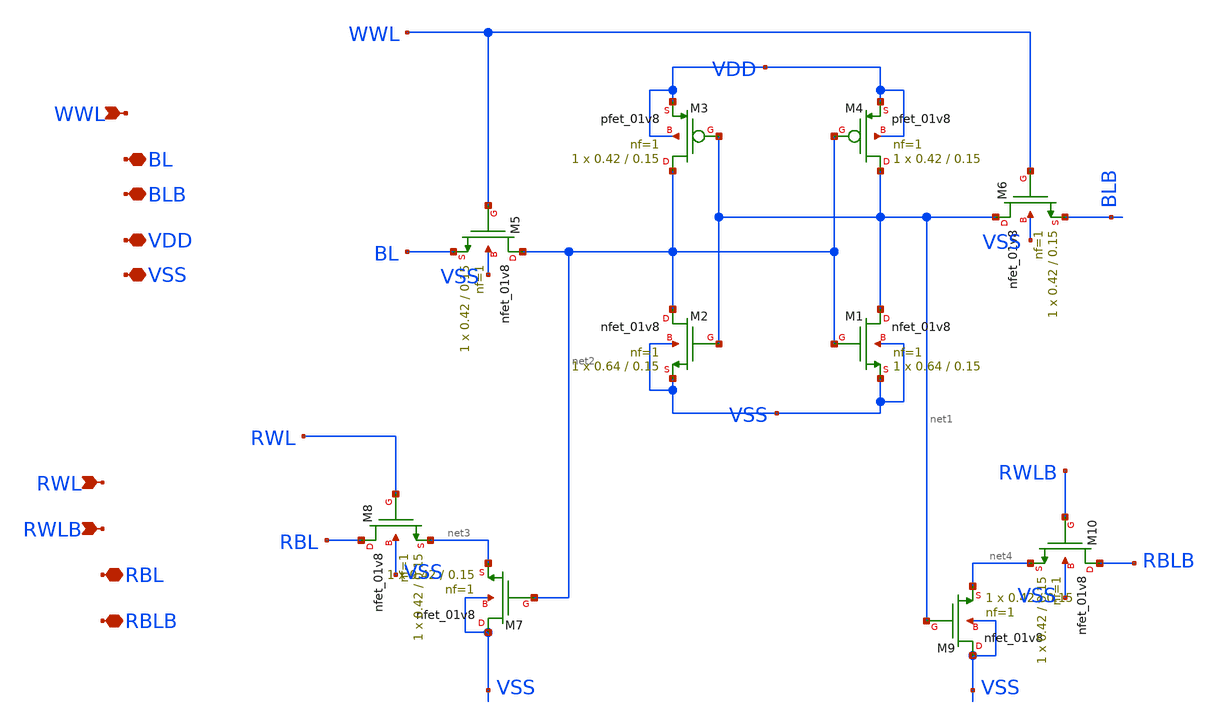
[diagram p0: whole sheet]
** sch_path: xschem/Integrated_bitcell/10T_SRAM_bitcell.sch
**.subckt 10T_SRAM_bitcell BL BLB VDD VSS RBL RBLB WWL RWL RWLB
*.iopin BL
*.iopin BLB
*.iopin VDD
*.iopin VSS
*.iopin RBL
*.iopin RBLB
*.ipin WWL
*.ipin RWL
*.ipin RWLB
XM1 net1 net2 VSS VSS sky130_fd_pr__nfet_01v8 L=0.15 W=0.64 nf=1 ad='int((nf+1)/2) * W/nf * 0.29' as='int((nf+2)/2) * W/nf * 0.29'
+ pd='2*int((nf+1)/2) * (W/nf + 0.29)' ps='2*int((nf+2)/2) * (W/nf + 0.29)' nrd='0.29 / W' nrs='0.29 / W'
+ sa=0 sb=0 sd=0 mult=1 m=1
XM2 net2 net1 VSS VSS sky130_fd_pr__nfet_01v8 L=0.15 W=0.64 nf=1 ad='int((nf+1)/2) * W/nf * 0.29' as='int((nf+2)/2) * W/nf * 0.29'
+ pd='2*int((nf+1)/2) * (W/nf + 0.29)' ps='2*int((nf+2)/2) * (W/nf + 0.29)' nrd='0.29 / W' nrs='0.29 / W'
+ sa=0 sb=0 sd=0 mult=1 m=1
XM3 net2 net1 VDD VDD sky130_fd_pr__pfet_01v8 L=0.15 W=0.42 nf=1 ad='int((nf+1)/2) * W/nf * 0.29' as='int((nf+2)/2) * W/nf * 0.29'
+ pd='2*int((nf+1)/2) * (W/nf + 0.29)' ps='2*int((nf+2)/2) * (W/nf + 0.29)' nrd='0.29 / W' nrs='0.29 / W'
+ sa=0 sb=0 sd=0 mult=1 m=1
XM4 net1 net2 VDD VDD sky130_fd_pr__pfet_01v8 L=0.15 W=0.42 nf=1 ad='int((nf+1)/2) * W/nf * 0.29' as='int((nf+2)/2) * W/nf * 0.29'
+ pd='2*int((nf+1)/2) * (W/nf + 0.29)' ps='2*int((nf+2)/2) * (W/nf + 0.29)' nrd='0.29 / W' nrs='0.29 / W'
+ sa=0 sb=0 sd=0 mult=1 m=1
XM6 net1 WWL BLB VSS sky130_fd_pr__nfet_01v8 L=0.15 W=0.42 nf=1 ad='int((nf+1)/2) * W/nf * 0.29' as='int((nf+2)/2) * W/nf * 0.29'
+ pd='2*int((nf+1)/2) * (W/nf + 0.29)' ps='2*int((nf+2)/2) * (W/nf + 0.29)' nrd='0.29 / W' nrs='0.29 / W'
+ sa=0 sb=0 sd=0 mult=1 m=1
XM5 net2 WWL BL VSS sky130_fd_pr__nfet_01v8 L=0.15 W=0.42 nf=1 ad='int((nf+1)/2) * W/nf * 0.29' as='int((nf+2)/2) * W/nf * 0.29'
+ pd='2*int((nf+1)/2) * (W/nf + 0.29)' ps='2*int((nf+2)/2) * (W/nf + 0.29)' nrd='0.29 / W' nrs='0.29 / W'
+ sa=0 sb=0 sd=0 mult=1 m=1
XM7 VSS net2 net3 VSS sky130_fd_pr__nfet_01v8 L=0.15 W=0.42 nf=1 ad='int((nf+1)/2) * W/nf * 0.29' as='int((nf+2)/2) * W/nf * 0.29'
+ pd='2*int((nf+1)/2) * (W/nf + 0.29)' ps='2*int((nf+2)/2) * (W/nf + 0.29)' nrd='0.29 / W' nrs='0.29 / W'
+ sa=0 sb=0 sd=0 mult=1 m=1
XM8 RBL RWL net3 VSS sky130_fd_pr__nfet_01v8 L=0.15 W=0.42 nf=1 ad='int((nf+1)/2) * W/nf * 0.29' as='int((nf+2)/2) * W/nf * 0.29'
+ pd='2*int((nf+1)/2) * (W/nf + 0.29)' ps='2*int((nf+2)/2) * (W/nf + 0.29)' nrd='0.29 / W' nrs='0.29 / W'
+ sa=0 sb=0 sd=0 mult=1 m=1
XM9 VSS net1 net4 VSS sky130_fd_pr__nfet_01v8 L=0.15 W=0.42 nf=1 ad='int((nf+1)/2) * W/nf * 0.29' as='int((nf+2)/2) * W/nf * 0.29'
+ pd='2*int((nf+1)/2) * (W/nf + 0.29)' ps='2*int((nf+2)/2) * (W/nf + 0.29)' nrd='0.29 / W' nrs='0.29 / W'
+ sa=0 sb=0 sd=0 mult=1 m=1
XM10 RBLB RWLB net4 VSS sky130_fd_pr__nfet_01v8 L=0.15 W=0.42 nf=1 ad='int((nf+1)/2) * W/nf * 0.29' as='int((nf+2)/2) * W/nf * 0.29'
+ pd='2*int((nf+1)/2) * (W/nf + 0.29)' ps='2*int((nf+2)/2) * (W/nf + 0.29)' nrd='0.29 / W' nrs='0.29 / W'
+ sa=0 sb=0 sd=0 mult=1 m=1
**.ends
.end
